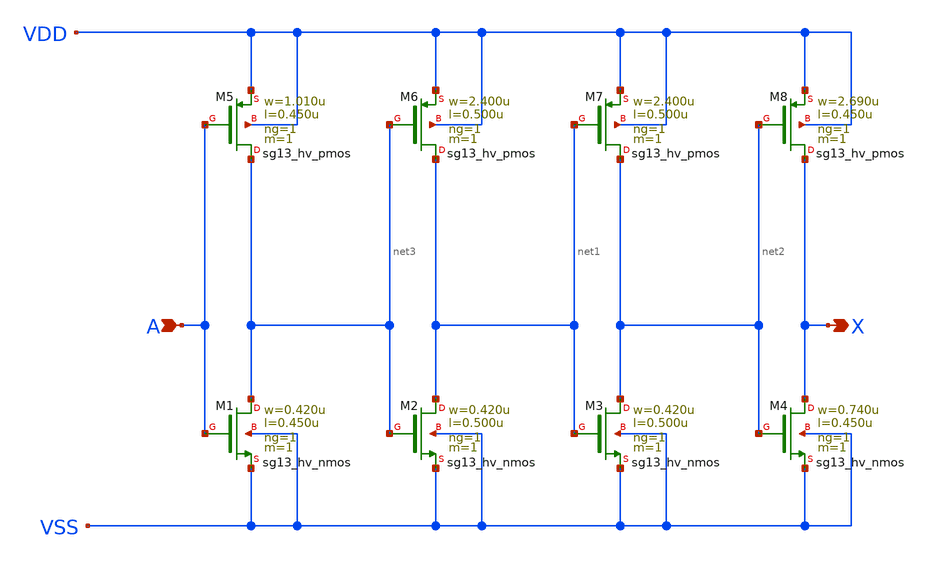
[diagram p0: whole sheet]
** sch_path: ihp-sg13g2/libs.ref/sg13g2_stdcell_hv/sch/xschem/sg13g2_hv_dlygate4sd3_1.sch
* Copyright 2023 IHP PDK Authors
* Licensed under the Apache License, Version 2.0 (the "License");
* you may not use this file except in compliance with the License.
* You may obtain a copy of the License at
* https://www.apache.org/licenses/LICENSE-2.0
* Unless required by applicable law or agreed to in writing, software
* distributed under the License is distributed on an "AS IS" BASIS,
* WITHOUT WARRANTIES OR CONDITIONS OF ANY KIND, either express or implied.
* See the License for the specific language governing permissions and
* limitations under the License.
**.subckt sg13g2_hv_dlygate4sd3_1 A X
*.ipin A
*.opin X
XM1 net3 A VSS VSS sg13_hv_nmos w=0.420u l=0.450u ng=1 m=1 mm_ok=1
XM2 net1 net3 VSS VSS sg13_hv_nmos w=0.420u l=0.500u ng=1 m=1 mm_ok=1
XM3 net2 net1 VSS VSS sg13_hv_nmos w=0.420u l=0.500u ng=1 m=1 mm_ok=1
XM4 X net2 VSS VSS sg13_hv_nmos w=0.740u l=0.450u ng=1 m=1 mm_ok=1
XM5 net3 A VDD VDD sg13_hv_pmos w=1.010u l=0.450u ng=1 m=1 mm_ok=1
XM6 net1 net3 VDD VDD sg13_hv_pmos w=2.400u l=0.500u ng=1 m=1 mm_ok=1
XM7 net2 net1 VDD VDD sg13_hv_pmos w=2.400u l=0.500u ng=1 m=1 mm_ok=1
XM8 X net2 VDD VDD sg13_hv_pmos w=2.690u l=0.450u ng=1 m=1 mm_ok=1
**.ends
.end
